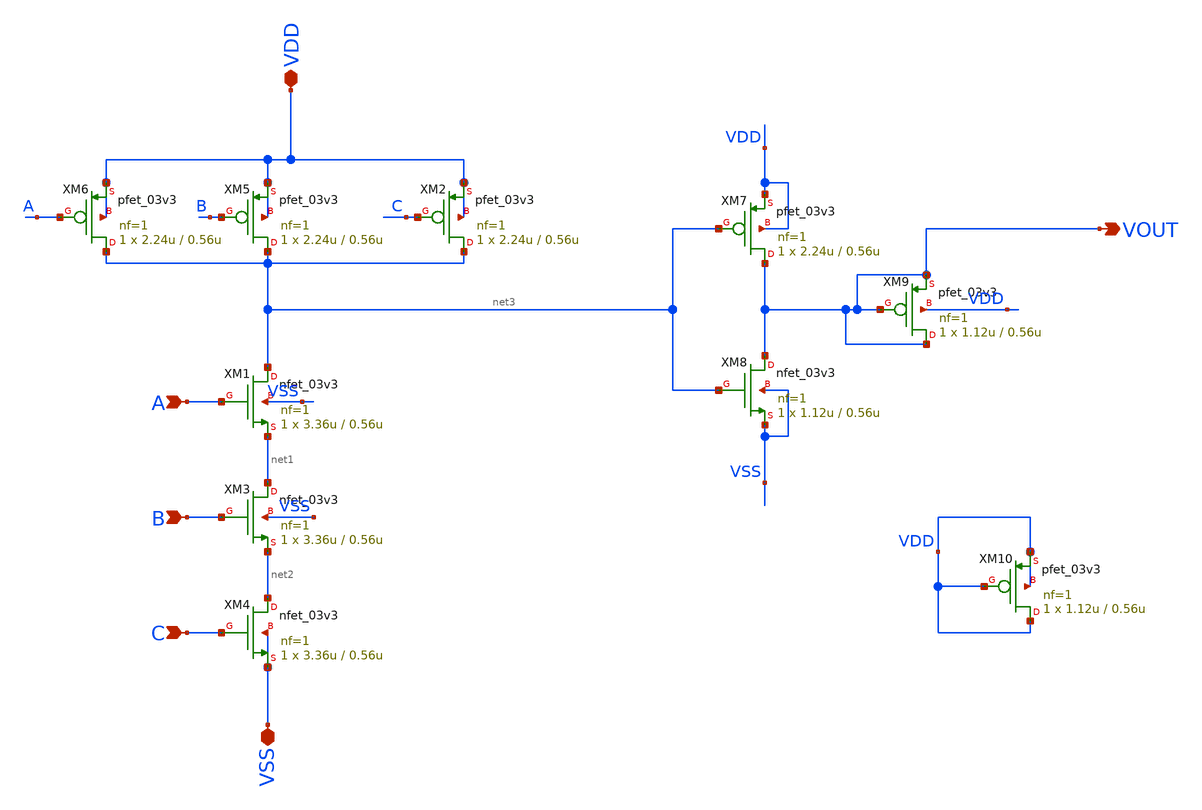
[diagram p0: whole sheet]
** sch_path: PLL-main/schematic/xschem/3_inp_AND.sch
**.subckt 3_inp_AND VSS VDD A B C VOUT
*.iopin VSS
*.iopin VDD
*.ipin A
*.ipin B
*.ipin C
*.opin VOUT
XM1 net3 A net1 VSS nfet_03v3 L=0.56u W=3.36u nf=1 ad='int((nf+1)/2) * W/nf * 0.18u' as='int((nf+2)/2) * W/nf * 0.18u'
+ pd='2*int((nf+1)/2) * (W/nf + 0.18u)' ps='2*int((nf+2)/2) * (W/nf + 0.18u)' nrd='0.18u / W' nrs='0.18u / W'
+ sa=0 sb=0 sd=0 m=1
XM2 net3 C VDD VDD pfet_03v3 L=0.56u W=2.24u nf=1 ad='int((nf+1)/2) * W/nf * 0.18u' as='int((nf+2)/2) * W/nf * 0.18u'
+ pd='2*int((nf+1)/2) * (W/nf + 0.18u)' ps='2*int((nf+2)/2) * (W/nf + 0.18u)' nrd='0.18u / W' nrs='0.18u / W'
+ sa=0 sb=0 sd=0 m=1
XM3 net1 B net2 VSS nfet_03v3 L=0.56u W=3.36u nf=1 ad='int((nf+1)/2) * W/nf * 0.18u' as='int((nf+2)/2) * W/nf * 0.18u'
+ pd='2*int((nf+1)/2) * (W/nf + 0.18u)' ps='2*int((nf+2)/2) * (W/nf + 0.18u)' nrd='0.18u / W' nrs='0.18u / W'
+ sa=0 sb=0 sd=0 m=1
XM4 net2 C VSS VSS nfet_03v3 L=0.56u W=3.36u nf=1 ad='int((nf+1)/2) * W/nf * 0.18u' as='int((nf+2)/2) * W/nf * 0.18u'
+ pd='2*int((nf+1)/2) * (W/nf + 0.18u)' ps='2*int((nf+2)/2) * (W/nf + 0.18u)' nrd='0.18u / W' nrs='0.18u / W'
+ sa=0 sb=0 sd=0 m=1
XM5 net3 B VDD VDD pfet_03v3 L=0.56u W=2.24u nf=1 ad='int((nf+1)/2) * W/nf * 0.18u' as='int((nf+2)/2) * W/nf * 0.18u'
+ pd='2*int((nf+1)/2) * (W/nf + 0.18u)' ps='2*int((nf+2)/2) * (W/nf + 0.18u)' nrd='0.18u / W' nrs='0.18u / W'
+ sa=0 sb=0 sd=0 m=1
XM6 net3 A VDD VDD pfet_03v3 L=0.56u W=2.24u nf=1 ad='int((nf+1)/2) * W/nf * 0.18u' as='int((nf+2)/2) * W/nf * 0.18u'
+ pd='2*int((nf+1)/2) * (W/nf + 0.18u)' ps='2*int((nf+2)/2) * (W/nf + 0.18u)' nrd='0.18u / W' nrs='0.18u / W'
+ sa=0 sb=0 sd=0 m=1
XM7 VOUT net3 VDD VDD pfet_03v3 L=0.56u W=2.24u nf=1 ad='int((nf+1)/2) * W/nf * 0.18u' as='int((nf+2)/2) * W/nf * 0.18u'
+ pd='2*int((nf+1)/2) * (W/nf + 0.18u)' ps='2*int((nf+2)/2) * (W/nf + 0.18u)' nrd='0.18u / W' nrs='0.18u / W'
+ sa=0 sb=0 sd=0 m=1
XM8 VOUT net3 VSS VSS nfet_03v3 L=0.56u W=1.12u nf=1 ad='int((nf+1)/2) * W/nf * 0.18u' as='int((nf+2)/2) * W/nf * 0.18u'
+ pd='2*int((nf+1)/2) * (W/nf + 0.18u)' ps='2*int((nf+2)/2) * (W/nf + 0.18u)' nrd='0.18u / W' nrs='0.18u / W'
+ sa=0 sb=0 sd=0 m=1
XM9 VOUT VOUT VOUT VDD pfet_03v3 L=0.56u W=1.12u nf=1 ad='int((nf+1)/2) * W/nf * 0.18u' as='int((nf+2)/2) * W/nf * 0.18u'
+ pd='2*int((nf+1)/2) * (W/nf + 0.18u)' ps='2*int((nf+2)/2) * (W/nf + 0.18u)' nrd='0.18u / W' nrs='0.18u / W'
+ sa=0 sb=0 sd=0 m=1
XM10 VDD VDD VDD VDD pfet_03v3 L=0.56u W=1.12u nf=1 ad='int((nf+1)/2) * W/nf * 0.18u' as='int((nf+2)/2) * W/nf * 0.18u'
+ pd='2*int((nf+1)/2) * (W/nf + 0.18u)' ps='2*int((nf+2)/2) * (W/nf + 0.18u)' nrd='0.18u / W' nrs='0.18u / W'
+ sa=0 sb=0 sd=0 m=1
**.ends
.end
